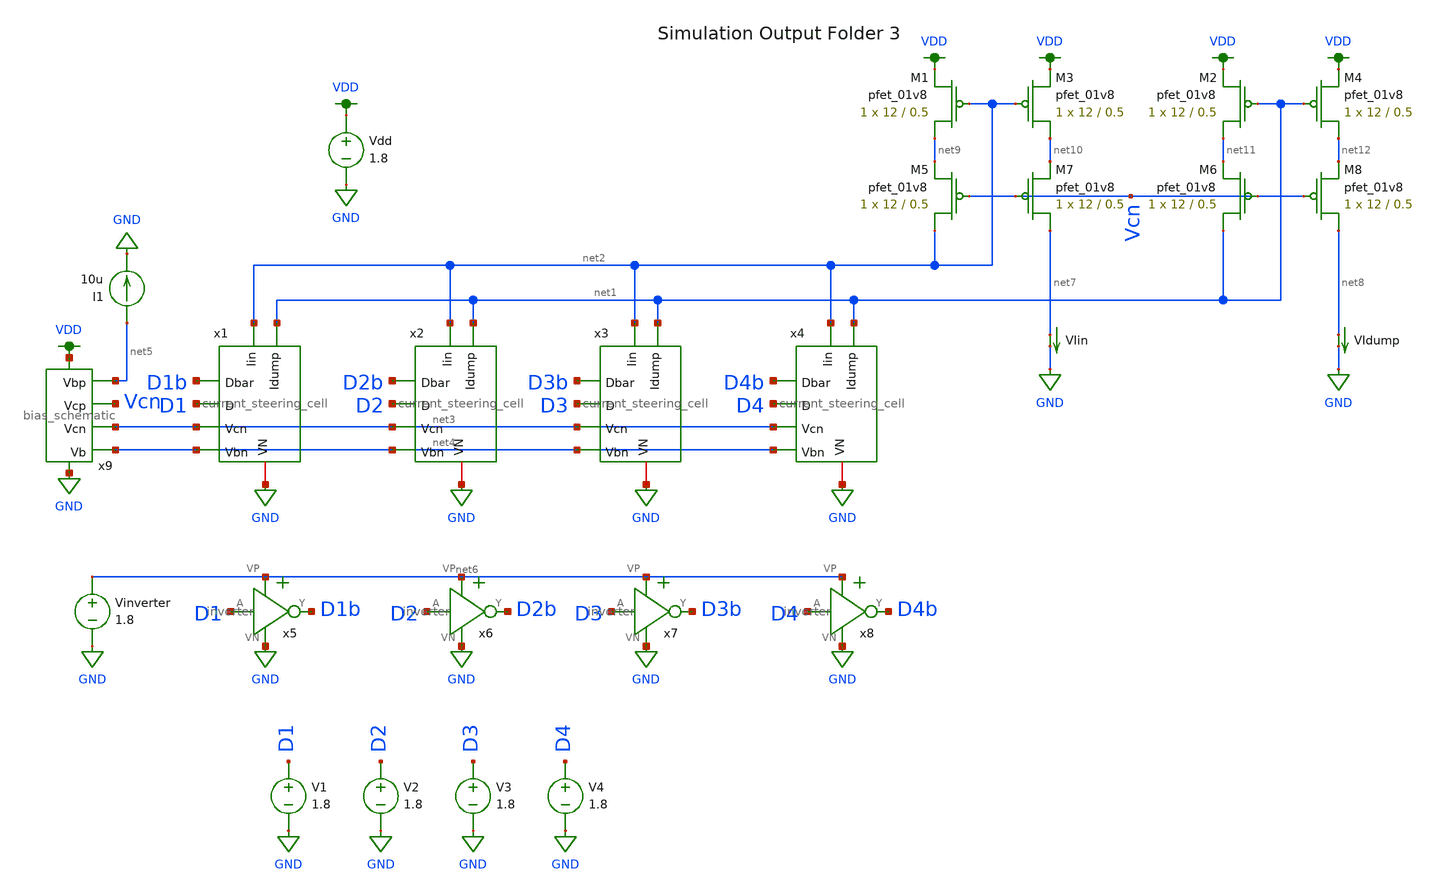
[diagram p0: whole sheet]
** sch_path: xschem/current_steering_testbenches/current_steering_testbench_pmos_cascode_mirror.sch
**.subckt current_steering_testbench_pmos_cascode_mirror
V1 D1 GND 1.8
V2 D2 GND 1.8
V3 D3 GND 1.8
V4 D4 GND 1.8
I1 net5 GND 10u
VIin net7 GND 0
.save i(viin)
VIdump net8 GND 0
.save i(vidump)
Vdd VDD GND 1.8
Vinverter net6 GND 1.8
XM1 net9 net2 VDD VDD sky130_fd_pr__pfet_01v8 L=0.5 W=12 nf=1 ad='int((nf+1)/2) * W/nf * 0.29' as='int((nf+2)/2) * W/nf * 0.29'
+ pd='2*int((nf+1)/2) * (W/nf + 0.29)' ps='2*int((nf+2)/2) * (W/nf + 0.29)' nrd='0.29 / W' nrs='0.29 / W'
+ sa=0 sb=0 sd=0 mult=1 m=1
XM2 net11 net1 VDD VDD sky130_fd_pr__pfet_01v8 L=0.5 W=12 nf=1 ad='int((nf+1)/2) * W/nf * 0.29' as='int((nf+2)/2) * W/nf * 0.29'
+ pd='2*int((nf+1)/2) * (W/nf + 0.29)' ps='2*int((nf+2)/2) * (W/nf + 0.29)' nrd='0.29 / W' nrs='0.29 / W'
+ sa=0 sb=0 sd=0 mult=1 m=1
XM3 net10 net2 VDD VDD sky130_fd_pr__pfet_01v8 L=0.5 W=12 nf=1 ad='int((nf+1)/2) * W/nf * 0.29' as='int((nf+2)/2) * W/nf * 0.29'
+ pd='2*int((nf+1)/2) * (W/nf + 0.29)' ps='2*int((nf+2)/2) * (W/nf + 0.29)' nrd='0.29 / W' nrs='0.29 / W'
+ sa=0 sb=0 sd=0 mult=1 m=1
XM4 net12 net1 VDD VDD sky130_fd_pr__pfet_01v8 L=0.5 W=12 nf=1 ad='int((nf+1)/2) * W/nf * 0.29' as='int((nf+2)/2) * W/nf * 0.29'
+ pd='2*int((nf+1)/2) * (W/nf + 0.29)' ps='2*int((nf+2)/2) * (W/nf + 0.29)' nrd='0.29 / W' nrs='0.29 / W'
+ sa=0 sb=0 sd=0 mult=1 m=1
XM5 net2 Vcn net9 VDD sky130_fd_pr__pfet_01v8 L=0.5 W=12 nf=1 ad='int((nf+1)/2) * W/nf * 0.29' as='int((nf+2)/2) * W/nf * 0.29'
+ pd='2*int((nf+1)/2) * (W/nf + 0.29)' ps='2*int((nf+2)/2) * (W/nf + 0.29)' nrd='0.29 / W' nrs='0.29 / W'
+ sa=0 sb=0 sd=0 mult=1 m=1
XM6 net1 Vcn net11 VDD sky130_fd_pr__pfet_01v8 L=0.5 W=12 nf=1 ad='int((nf+1)/2) * W/nf * 0.29' as='int((nf+2)/2) * W/nf * 0.29'
+ pd='2*int((nf+1)/2) * (W/nf + 0.29)' ps='2*int((nf+2)/2) * (W/nf + 0.29)' nrd='0.29 / W' nrs='0.29 / W'
+ sa=0 sb=0 sd=0 mult=1 m=1
XM7 net7 Vcn net10 VDD sky130_fd_pr__pfet_01v8 L=0.5 W=12 nf=1 ad='int((nf+1)/2) * W/nf * 0.29' as='int((nf+2)/2) * W/nf * 0.29'
+ pd='2*int((nf+1)/2) * (W/nf + 0.29)' ps='2*int((nf+2)/2) * (W/nf + 0.29)' nrd='0.29 / W' nrs='0.29 / W'
+ sa=0 sb=0 sd=0 mult=1 m=1
XM8 net8 Vcn net12 VDD sky130_fd_pr__pfet_01v8 L=0.5 W=12 nf=1 ad='int((nf+1)/2) * W/nf * 0.29' as='int((nf+2)/2) * W/nf * 0.29'
+ pd='2*int((nf+1)/2) * (W/nf + 0.29)' ps='2*int((nf+2)/2) * (W/nf + 0.29)' nrd='0.29 / W' nrs='0.29 / W'
+ sa=0 sb=0 sd=0 mult=1 m=1
x1 net2 net1 D1b D1 net3 net4 GND current_steering_cell
x2 net2 net1 D2b D2 net3 net4 GND current_steering_cell
x3 net2 net1 D3b D3 net3 net4 GND current_steering_cell
x4 net2 net1 D4b D4 net3 net4 GND current_steering_cell
x5 net6 D1 D1b GND inverter
x6 net6 D2 D2b GND inverter
x7 net6 D3 D3b GND inverter
x8 net6 D4 D4b GND inverter
x9 VDD net5 Vcn net3 GND net4 bias_schematic
**** begin user architecture code

.save all
.control
set wr_vecnames
set wr_singlescale

let mc_runs = 10
let run = 1
dowhile run <= mc_runs

  let code = 0
  while code <= 4
    let d1 = code >= 1
    let d2 = code >= 2
    let d3 = code >= 3
    let d4 = code >= 4

    alter V1 $&d1
    alter V2 $&d2
    alter V3 $&d3
    alter V4 $&d4
    save all
    op

    wrdata ~/dev/git/magic-dds/simulations/current_steering_dac/3/ieeeDAC_{$&run}.txt code v(D1) v(D1b)
+ i(VIin) i(VIdump)
    if code eq 0
      set appendwrite
      set wr_vecnames = FALSE
    end
    let code = code + 1
  end
  reset
  set appendwrite = FALSE
  set wr_vecnames
  let run = run + 1
end
.endc


.option wnflag=1
.param MC_SWITCH=1.0
.lib ~/skywater/skywater-pdk/libraries/sky130_fd_pr_ngspice/latest/models/sky130.lib.spice tt

**** end user architecture code
**.ends

* expanding   symbol:  /home/madvlsi/dev/git/magic-dds/xschem/current_steering_cell.sym # of pins=7
** sym_path: xschem/current_steering_cell.sym
** sch_path: xschem/current_steering_cell.sch
.subckt current_steering_cell Iin Idump Dbar D Vcn Vbn VN
*.iopin VN
*.ipin D
*.ipin Dbar
*.ipin Vcn
*.ipin Iin
*.ipin Idump
*.ipin Vbn
XM1 Iin D net1 GND sky130_fd_pr__nfet_01v8 L=0.5 W=12 nf=1 ad='int((nf+1)/2) * W/nf * 0.29' as='int((nf+2)/2) * W/nf * 0.29'
+ pd='2*int((nf+1)/2) * (W/nf + 0.29)' ps='2*int((nf+2)/2) * (W/nf + 0.29)' nrd='0.29 / W' nrs='0.29 / W'
+ sa=0 sb=0 sd=0 mult=1 m=1
XM2 Idump Dbar net1 GND sky130_fd_pr__nfet_01v8 L=0.5 W=12 nf=1 ad='int((nf+1)/2) * W/nf * 0.29' as='int((nf+2)/2) * W/nf * 0.29'
+ pd='2*int((nf+1)/2) * (W/nf + 0.29)' ps='2*int((nf+2)/2) * (W/nf + 0.29)' nrd='0.29 / W' nrs='0.29 / W'
+ sa=0 sb=0 sd=0 mult=1 m=1
XM3 net2 Vbn VN GND sky130_fd_pr__nfet_01v8 L=0.5 W=12 nf=1 ad='int((nf+1)/2) * W/nf * 0.29' as='int((nf+2)/2) * W/nf * 0.29'
+ pd='2*int((nf+1)/2) * (W/nf + 0.29)' ps='2*int((nf+2)/2) * (W/nf + 0.29)' nrd='0.29 / W' nrs='0.29 / W'
+ sa=0 sb=0 sd=0 mult=1 m=1
XM4 net1 Vcn net2 GND sky130_fd_pr__nfet_01v8 L=0.5 W=12 nf=1 ad='int((nf+1)/2) * W/nf * 0.29' as='int((nf+2)/2) * W/nf * 0.29'
+ pd='2*int((nf+1)/2) * (W/nf + 0.29)' ps='2*int((nf+2)/2) * (W/nf + 0.29)' nrd='0.29 / W' nrs='0.29 / W'
+ sa=0 sb=0 sd=0 mult=1 m=1
.ends


* expanding   symbol:  /home/madvlsi/dev/git/magic-dds/xschem/other_project_files/inverter.sym # of
*+ pins=4
** sym_path: xschem/other_project_files/inverter.sym
** sch_path: xschem/other_project_files/inverter.sch
.subckt inverter VP A Y VN
*.iopin VP
*.iopin VN
*.ipin A
*.opin Y
XM1 Y A VN VN sky130_fd_pr__nfet_01v8 L=0.15 W=1 nf=1 ad='int((nf+1)/2) * W/nf * 0.29' as='int((nf+2)/2) * W/nf * 0.29'
+ pd='2*int((nf+1)/2) * (W/nf + 0.29)' ps='2*int((nf+2)/2) * (W/nf + 0.29)' nrd='0.29 / W' nrs='0.29 / W'
+ sa=0 sb=0 sd=0 mult=1 m=1
XM2 Y A VP VP sky130_fd_pr__pfet_01v8 L=0.15 W=4 nf=1 ad='int((nf+1)/2) * W/nf * 0.29' as='int((nf+2)/2) * W/nf * 0.29'
+ pd='2*int((nf+1)/2) * (W/nf + 0.29)' ps='2*int((nf+2)/2) * (W/nf + 0.29)' nrd='0.29 / W' nrs='0.29 / W'
+ sa=0 sb=0 sd=0 mult=1 m=1
.ends


* expanding   symbol:  /home/madvlsi/dev/git/magic-dds/xschem/other_project_files/bias_schematic.sym
*+ # of pins=6
** sym_path: xschem/other_project_files/bias_schematic.sym
** sch_path: xschem/other_project_files/bias_schematic.sch
.subckt bias_schematic VP Vbp Vcp Vcn VN Vb
*.iopin VP
*.iopin VN
*.opin Vcp
*.iopin Vbp
*.opin Vcn
*.opin Vb
XM1a net2 net2 net1 GND sky130_fd_pr__nfet_01v8 L=0.5 W=3 nf=1 ad='int((nf+1)/2) * W/nf * 0.29' as='int((nf+2)/2) * W/nf * 0.29'
+ pd='2*int((nf+1)/2) * (W/nf + 0.29)' ps='2*int((nf+2)/2) * (W/nf + 0.29)' nrd='0.29 / W' nrs='0.29 / W'
+ sa=0 sb=0 sd=0 mult=1 m=1
XM1b net2 net2 net1 GND sky130_fd_pr__nfet_01v8 L=0.5 W=3 nf=1 ad='int((nf+1)/2) * W/nf * 0.29' as='int((nf+2)/2) * W/nf * 0.29'
+ pd='2*int((nf+1)/2) * (W/nf + 0.29)' ps='2*int((nf+2)/2) * (W/nf + 0.29)' nrd='0.29 / W' nrs='0.29 / W'
+ sa=0 sb=0 sd=0 mult=1 m=1
XM1c net2 net2 net1 GND sky130_fd_pr__nfet_01v8 L=0.5 W=3 nf=1 ad='int((nf+1)/2) * W/nf * 0.29' as='int((nf+2)/2) * W/nf * 0.29'
+ pd='2*int((nf+1)/2) * (W/nf + 0.29)' ps='2*int((nf+2)/2) * (W/nf + 0.29)' nrd='0.29 / W' nrs='0.29 / W'
+ sa=0 sb=0 sd=0 mult=1 m=1
XM1d net2 net2 net1 GND sky130_fd_pr__nfet_01v8 L=0.5 W=3 nf=1 ad='int((nf+1)/2) * W/nf * 0.29' as='int((nf+2)/2) * W/nf * 0.29'
+ pd='2*int((nf+1)/2) * (W/nf + 0.29)' ps='2*int((nf+2)/2) * (W/nf + 0.29)' nrd='0.29 / W' nrs='0.29 / W'
+ sa=0 sb=0 sd=0 mult=1 m=1
XM2a VN net2 net1 GND sky130_fd_pr__nfet_01v8 L=0.5 W=3 nf=1 ad='int((nf+1)/2) * W/nf * 0.29' as='int((nf+2)/2) * W/nf * 0.29'
+ pd='2*int((nf+1)/2) * (W/nf + 0.29)' ps='2*int((nf+2)/2) * (W/nf + 0.29)' nrd='0.29 / W' nrs='0.29 / W'
+ sa=0 sb=0 sd=0 mult=1 m=1
XM2b VN net2 net1 GND sky130_fd_pr__nfet_01v8 L=0.5 W=3 nf=1 ad='int((nf+1)/2) * W/nf * 0.29' as='int((nf+2)/2) * W/nf * 0.29'
+ pd='2*int((nf+1)/2) * (W/nf + 0.29)' ps='2*int((nf+2)/2) * (W/nf + 0.29)' nrd='0.29 / W' nrs='0.29 / W'
+ sa=0 sb=0 sd=0 mult=1 m=1
XM2c VN net2 net1 GND sky130_fd_pr__nfet_01v8 L=0.5 W=3 nf=1 ad='int((nf+1)/2) * W/nf * 0.29' as='int((nf+2)/2) * W/nf * 0.29'
+ pd='2*int((nf+1)/2) * (W/nf + 0.29)' ps='2*int((nf+2)/2) * (W/nf + 0.29)' nrd='0.29 / W' nrs='0.29 / W'
+ sa=0 sb=0 sd=0 mult=1 m=1
XM2d VN net2 net1 GND sky130_fd_pr__nfet_01v8 L=0.5 W=3 nf=1 ad='int((nf+1)/2) * W/nf * 0.29' as='int((nf+2)/2) * W/nf * 0.29'
+ pd='2*int((nf+1)/2) * (W/nf + 0.29)' ps='2*int((nf+2)/2) * (W/nf + 0.29)' nrd='0.29 / W' nrs='0.29 / W'
+ sa=0 sb=0 sd=0 mult=1 m=1
XM3a net2 Vbp net7 VDD sky130_fd_pr__pfet_01v8 L=0.5 W=3 nf=1 ad='int((nf+1)/2) * W/nf * 0.29' as='int((nf+2)/2) * W/nf * 0.29'
+ pd='2*int((nf+1)/2) * (W/nf + 0.29)' ps='2*int((nf+2)/2) * (W/nf + 0.29)' nrd='0.29 / W' nrs='0.29 / W'
+ sa=0 sb=0 sd=0 mult=1 m=1
XM3b net7 Vbp net6 VDD sky130_fd_pr__pfet_01v8 L=0.5 W=3 nf=1 ad='int((nf+1)/2) * W/nf * 0.29' as='int((nf+2)/2) * W/nf * 0.29'
+ pd='2*int((nf+1)/2) * (W/nf + 0.29)' ps='2*int((nf+2)/2) * (W/nf + 0.29)' nrd='0.29 / W' nrs='0.29 / W'
+ sa=0 sb=0 sd=0 mult=1 m=1
XM3c net6 Vbp net5 VDD sky130_fd_pr__pfet_01v8 L=0.5 W=3 nf=1 ad='int((nf+1)/2) * W/nf * 0.29' as='int((nf+2)/2) * W/nf * 0.29'
+ pd='2*int((nf+1)/2) * (W/nf + 0.29)' ps='2*int((nf+2)/2) * (W/nf + 0.29)' nrd='0.29 / W' nrs='0.29 / W'
+ sa=0 sb=0 sd=0 mult=1 m=1
XM3d net5 Vbp VP VDD sky130_fd_pr__pfet_01v8 L=0.5 W=3 nf=1 ad='int((nf+1)/2) * W/nf * 0.29' as='int((nf+2)/2) * W/nf * 0.29'
+ pd='2*int((nf+1)/2) * (W/nf + 0.29)' ps='2*int((nf+2)/2) * (W/nf + 0.29)' nrd='0.29 / W' nrs='0.29 / W'
+ sa=0 sb=0 sd=0 mult=1 m=1
XM4a Vcn Vbp VP VDD sky130_fd_pr__pfet_01v8 L=0.5 W=3 nf=1 ad='int((nf+1)/2) * W/nf * 0.29' as='int((nf+2)/2) * W/nf * 0.29'
+ pd='2*int((nf+1)/2) * (W/nf + 0.29)' ps='2*int((nf+2)/2) * (W/nf + 0.29)' nrd='0.29 / W' nrs='0.29 / W'
+ sa=0 sb=0 sd=0 mult=1 m=1
XM4b Vcn Vbp VP VDD sky130_fd_pr__pfet_01v8 L=0.5 W=3 nf=1 ad='int((nf+1)/2) * W/nf * 0.29' as='int((nf+2)/2) * W/nf * 0.29'
+ pd='2*int((nf+1)/2) * (W/nf + 0.29)' ps='2*int((nf+2)/2) * (W/nf + 0.29)' nrd='0.29 / W' nrs='0.29 / W'
+ sa=0 sb=0 sd=0 mult=1 m=1
XM4c Vcn Vbp VP VDD sky130_fd_pr__pfet_01v8 L=0.5 W=3 nf=1 ad='int((nf+1)/2) * W/nf * 0.29' as='int((nf+2)/2) * W/nf * 0.29'
+ pd='2*int((nf+1)/2) * (W/nf + 0.29)' ps='2*int((nf+2)/2) * (W/nf + 0.29)' nrd='0.29 / W' nrs='0.29 / W'
+ sa=0 sb=0 sd=0 mult=1 m=1
XM4d Vcn Vbp VP VDD sky130_fd_pr__pfet_01v8 L=0.5 W=3 nf=1 ad='int((nf+1)/2) * W/nf * 0.29' as='int((nf+2)/2) * W/nf * 0.29'
+ pd='2*int((nf+1)/2) * (W/nf + 0.29)' ps='2*int((nf+2)/2) * (W/nf + 0.29)' nrd='0.29 / W' nrs='0.29 / W'
+ sa=0 sb=0 sd=0 mult=1 m=1
XM11a VP Vbp Vbp VDD sky130_fd_pr__pfet_01v8 L=0.5 W=3 nf=1 ad='int((nf+1)/2) * W/nf * 0.29' as='int((nf+2)/2) * W/nf * 0.29'
+ pd='2*int((nf+1)/2) * (W/nf + 0.29)' ps='2*int((nf+2)/2) * (W/nf + 0.29)' nrd='0.29 / W' nrs='0.29 / W'
+ sa=0 sb=0 sd=0 mult=1 m=1
XM11b VP Vbp Vbp VDD sky130_fd_pr__pfet_01v8 L=0.5 W=3 nf=1 ad='int((nf+1)/2) * W/nf * 0.29' as='int((nf+2)/2) * W/nf * 0.29'
+ pd='2*int((nf+1)/2) * (W/nf + 0.29)' ps='2*int((nf+2)/2) * (W/nf + 0.29)' nrd='0.29 / W' nrs='0.29 / W'
+ sa=0 sb=0 sd=0 mult=1 m=1
XM11c VP Vbp Vbp VDD sky130_fd_pr__pfet_01v8 L=0.5 W=3 nf=1 ad='int((nf+1)/2) * W/nf * 0.29' as='int((nf+2)/2) * W/nf * 0.29'
+ pd='2*int((nf+1)/2) * (W/nf + 0.29)' ps='2*int((nf+2)/2) * (W/nf + 0.29)' nrd='0.29 / W' nrs='0.29 / W'
+ sa=0 sb=0 sd=0 mult=1 m=1
XM11d VP Vbp Vbp VDD sky130_fd_pr__pfet_01v8 L=0.5 W=3 nf=1 ad='int((nf+1)/2) * W/nf * 0.29' as='int((nf+2)/2) * W/nf * 0.29'
+ pd='2*int((nf+1)/2) * (W/nf + 0.29)' ps='2*int((nf+2)/2) * (W/nf + 0.29)' nrd='0.29 / W' nrs='0.29 / W'
+ sa=0 sb=0 sd=0 mult=1 m=1
XM5a net1 Vcn Vcn GND sky130_fd_pr__nfet_01v8 L=0.5 W=3 nf=1 ad='int((nf+1)/2) * W/nf * 0.29' as='int((nf+2)/2) * W/nf * 0.29'
+ pd='2*int((nf+1)/2) * (W/nf + 0.29)' ps='2*int((nf+2)/2) * (W/nf + 0.29)' nrd='0.29 / W' nrs='0.29 / W'
+ sa=0 sb=0 sd=0 mult=1 m=1
XM5b net1 Vcn Vcn GND sky130_fd_pr__nfet_01v8 L=0.5 W=3 nf=1 ad='int((nf+1)/2) * W/nf * 0.29' as='int((nf+2)/2) * W/nf * 0.29'
+ pd='2*int((nf+1)/2) * (W/nf + 0.29)' ps='2*int((nf+2)/2) * (W/nf + 0.29)' nrd='0.29 / W' nrs='0.29 / W'
+ sa=0 sb=0 sd=0 mult=1 m=1
XM5c net1 Vcn Vcn GND sky130_fd_pr__nfet_01v8 L=0.5 W=3 nf=1 ad='int((nf+1)/2) * W/nf * 0.29' as='int((nf+2)/2) * W/nf * 0.29'
+ pd='2*int((nf+1)/2) * (W/nf + 0.29)' ps='2*int((nf+2)/2) * (W/nf + 0.29)' nrd='0.29 / W' nrs='0.29 / W'
+ sa=0 sb=0 sd=0 mult=1 m=1
XM5d net1 Vcn Vcn GND sky130_fd_pr__nfet_01v8 L=0.5 W=3 nf=1 ad='int((nf+1)/2) * W/nf * 0.29' as='int((nf+2)/2) * W/nf * 0.29'
+ pd='2*int((nf+1)/2) * (W/nf + 0.29)' ps='2*int((nf+2)/2) * (W/nf + 0.29)' nrd='0.29 / W' nrs='0.29 / W'
+ sa=0 sb=0 sd=0 mult=1 m=1
XM8a net10 Vb net3 GND sky130_fd_pr__nfet_01v8 L=0.5 W=3 nf=1 ad='int((nf+1)/2) * W/nf * 0.29' as='int((nf+2)/2) * W/nf * 0.29'
+ pd='2*int((nf+1)/2) * (W/nf + 0.29)' ps='2*int((nf+2)/2) * (W/nf + 0.29)' nrd='0.29 / W' nrs='0.29 / W'
+ sa=0 sb=0 sd=0 mult=1 m=1
XM8b net9 Vb net10 GND sky130_fd_pr__nfet_01v8 L=0.5 W=3 nf=1 ad='int((nf+1)/2) * W/nf * 0.29' as='int((nf+2)/2) * W/nf * 0.29'
+ pd='2*int((nf+1)/2) * (W/nf + 0.29)' ps='2*int((nf+2)/2) * (W/nf + 0.29)' nrd='0.29 / W' nrs='0.29 / W'
+ sa=0 sb=0 sd=0 mult=1 m=1
XM8c net8 Vb net9 GND sky130_fd_pr__nfet_01v8 L=0.5 W=3 nf=1 ad='int((nf+1)/2) * W/nf * 0.29' as='int((nf+2)/2) * W/nf * 0.29'
+ pd='2*int((nf+1)/2) * (W/nf + 0.29)' ps='2*int((nf+2)/2) * (W/nf + 0.29)' nrd='0.29 / W' nrs='0.29 / W'
+ sa=0 sb=0 sd=0 mult=1 m=1
XM8d VN Vb net8 GND sky130_fd_pr__nfet_01v8 L=0.5 W=3 nf=1 ad='int((nf+1)/2) * W/nf * 0.29' as='int((nf+2)/2) * W/nf * 0.29'
+ pd='2*int((nf+1)/2) * (W/nf + 0.29)' ps='2*int((nf+2)/2) * (W/nf + 0.29)' nrd='0.29 / W' nrs='0.29 / W'
+ sa=0 sb=0 sd=0 mult=1 m=1
XM6a net3 net3 net4 VDD sky130_fd_pr__pfet_01v8 L=0.5 W=3 nf=1 ad='int((nf+1)/2) * W/nf * 0.29' as='int((nf+2)/2) * W/nf * 0.29'
+ pd='2*int((nf+1)/2) * (W/nf + 0.29)' ps='2*int((nf+2)/2) * (W/nf + 0.29)' nrd='0.29 / W' nrs='0.29 / W'
+ sa=0 sb=0 sd=0 mult=1 m=1
XM6b net3 net3 net4 VDD sky130_fd_pr__pfet_01v8 L=0.5 W=3 nf=1 ad='int((nf+1)/2) * W/nf * 0.29' as='int((nf+2)/2) * W/nf * 0.29'
+ pd='2*int((nf+1)/2) * (W/nf + 0.29)' ps='2*int((nf+2)/2) * (W/nf + 0.29)' nrd='0.29 / W' nrs='0.29 / W'
+ sa=0 sb=0 sd=0 mult=1 m=1
XM6c net3 net3 net4 VDD sky130_fd_pr__pfet_01v8 L=0.5 W=3 nf=1 ad='int((nf+1)/2) * W/nf * 0.29' as='int((nf+2)/2) * W/nf * 0.29'
+ pd='2*int((nf+1)/2) * (W/nf + 0.29)' ps='2*int((nf+2)/2) * (W/nf + 0.29)' nrd='0.29 / W' nrs='0.29 / W'
+ sa=0 sb=0 sd=0 mult=1 m=1
XM6d net3 net3 net4 VDD sky130_fd_pr__pfet_01v8 L=0.5 W=3 nf=1 ad='int((nf+1)/2) * W/nf * 0.29' as='int((nf+2)/2) * W/nf * 0.29'
+ pd='2*int((nf+1)/2) * (W/nf + 0.29)' ps='2*int((nf+2)/2) * (W/nf + 0.29)' nrd='0.29 / W' nrs='0.29 / W'
+ sa=0 sb=0 sd=0 mult=1 m=1
XM7a net4 net3 VP VDD sky130_fd_pr__pfet_01v8 L=0.5 W=3 nf=1 ad='int((nf+1)/2) * W/nf * 0.29' as='int((nf+2)/2) * W/nf * 0.29'
+ pd='2*int((nf+1)/2) * (W/nf + 0.29)' ps='2*int((nf+2)/2) * (W/nf + 0.29)' nrd='0.29 / W' nrs='0.29 / W'
+ sa=0 sb=0 sd=0 mult=1 m=1
XM7b net4 net3 VP VDD sky130_fd_pr__pfet_01v8 L=0.5 W=3 nf=1 ad='int((nf+1)/2) * W/nf * 0.29' as='int((nf+2)/2) * W/nf * 0.29'
+ pd='2*int((nf+1)/2) * (W/nf + 0.29)' ps='2*int((nf+2)/2) * (W/nf + 0.29)' nrd='0.29 / W' nrs='0.29 / W'
+ sa=0 sb=0 sd=0 mult=1 m=1
XM7c net4 net3 VP VDD sky130_fd_pr__pfet_01v8 L=0.5 W=3 nf=1 ad='int((nf+1)/2) * W/nf * 0.29' as='int((nf+2)/2) * W/nf * 0.29'
+ pd='2*int((nf+1)/2) * (W/nf + 0.29)' ps='2*int((nf+2)/2) * (W/nf + 0.29)' nrd='0.29 / W' nrs='0.29 / W'
+ sa=0 sb=0 sd=0 mult=1 m=1
XM7d net4 net3 VP VDD sky130_fd_pr__pfet_01v8 L=0.5 W=3 nf=1 ad='int((nf+1)/2) * W/nf * 0.29' as='int((nf+2)/2) * W/nf * 0.29'
+ pd='2*int((nf+1)/2) * (W/nf + 0.29)' ps='2*int((nf+2)/2) * (W/nf + 0.29)' nrd='0.29 / W' nrs='0.29 / W'
+ sa=0 sb=0 sd=0 mult=1 m=1
XM10d net4 Vcp Vcp VDD sky130_fd_pr__pfet_01v8 L=0.5 W=3 nf=1 ad='int((nf+1)/2) * W/nf * 0.29' as='int((nf+2)/2) * W/nf * 0.29'
+ pd='2*int((nf+1)/2) * (W/nf + 0.29)' ps='2*int((nf+2)/2) * (W/nf + 0.29)' nrd='0.29 / W' nrs='0.29 / W'
+ sa=0 sb=0 sd=0 mult=1 m=1
XM10c net4 Vcp Vcp VDD sky130_fd_pr__pfet_01v8 L=0.5 W=3 nf=1 ad='int((nf+1)/2) * W/nf * 0.29' as='int((nf+2)/2) * W/nf * 0.29'
+ pd='2*int((nf+1)/2) * (W/nf + 0.29)' ps='2*int((nf+2)/2) * (W/nf + 0.29)' nrd='0.29 / W' nrs='0.29 / W'
+ sa=0 sb=0 sd=0 mult=1 m=1
XM10b net4 Vcp Vcp VDD sky130_fd_pr__pfet_01v8 L=0.5 W=3 nf=1 ad='int((nf+1)/2) * W/nf * 0.29' as='int((nf+2)/2) * W/nf * 0.29'
+ pd='2*int((nf+1)/2) * (W/nf + 0.29)' ps='2*int((nf+2)/2) * (W/nf + 0.29)' nrd='0.29 / W' nrs='0.29 / W'
+ sa=0 sb=0 sd=0 mult=1 m=1
XM10a net4 Vcp Vcp VDD sky130_fd_pr__pfet_01v8 L=0.5 W=3 nf=1 ad='int((nf+1)/2) * W/nf * 0.29' as='int((nf+2)/2) * W/nf * 0.29'
+ pd='2*int((nf+1)/2) * (W/nf + 0.29)' ps='2*int((nf+2)/2) * (W/nf + 0.29)' nrd='0.29 / W' nrs='0.29 / W'
+ sa=0 sb=0 sd=0 mult=1 m=1
XM9a VN Vb Vcp GND sky130_fd_pr__nfet_01v8 L=0.5 W=3 nf=1 ad='int((nf+1)/2) * W/nf * 0.29' as='int((nf+2)/2) * W/nf * 0.29'
+ pd='2*int((nf+1)/2) * (W/nf + 0.29)' ps='2*int((nf+2)/2) * (W/nf + 0.29)' nrd='0.29 / W' nrs='0.29 / W'
+ sa=0 sb=0 sd=0 mult=1 m=1
XM9b VN Vb Vcp GND sky130_fd_pr__nfet_01v8 L=0.5 W=3 nf=1 ad='int((nf+1)/2) * W/nf * 0.29' as='int((nf+2)/2) * W/nf * 0.29'
+ pd='2*int((nf+1)/2) * (W/nf + 0.29)' ps='2*int((nf+2)/2) * (W/nf + 0.29)' nrd='0.29 / W' nrs='0.29 / W'
+ sa=0 sb=0 sd=0 mult=1 m=1
XM9c VN Vb Vcp GND sky130_fd_pr__nfet_01v8 L=0.5 W=3 nf=1 ad='int((nf+1)/2) * W/nf * 0.29' as='int((nf+2)/2) * W/nf * 0.29'
+ pd='2*int((nf+1)/2) * (W/nf + 0.29)' ps='2*int((nf+2)/2) * (W/nf + 0.29)' nrd='0.29 / W' nrs='0.29 / W'
+ sa=0 sb=0 sd=0 mult=1 m=1
XM9d VN Vb Vcp GND sky130_fd_pr__nfet_01v8 L=0.5 W=3 nf=1 ad='int((nf+1)/2) * W/nf * 0.29' as='int((nf+2)/2) * W/nf * 0.29'
+ pd='2*int((nf+1)/2) * (W/nf + 0.29)' ps='2*int((nf+2)/2) * (W/nf + 0.29)' nrd='0.29 / W' nrs='0.29 / W'
+ sa=0 sb=0 sd=0 mult=1 m=1
XM12a VN Vb Vb GND sky130_fd_pr__nfet_01v8 L=0.5 W=3 nf=1 ad='int((nf+1)/2) * W/nf * 0.29' as='int((nf+2)/2) * W/nf * 0.29'
+ pd='2*int((nf+1)/2) * (W/nf + 0.29)' ps='2*int((nf+2)/2) * (W/nf + 0.29)' nrd='0.29 / W' nrs='0.29 / W'
+ sa=0 sb=0 sd=0 mult=1 m=1
XM12b VN Vb Vb GND sky130_fd_pr__nfet_01v8 L=0.5 W=3 nf=1 ad='int((nf+1)/2) * W/nf * 0.29' as='int((nf+2)/2) * W/nf * 0.29'
+ pd='2*int((nf+1)/2) * (W/nf + 0.29)' ps='2*int((nf+2)/2) * (W/nf + 0.29)' nrd='0.29 / W' nrs='0.29 / W'
+ sa=0 sb=0 sd=0 mult=1 m=1
XM12c VN Vb Vb GND sky130_fd_pr__nfet_01v8 L=0.5 W=3 nf=1 ad='int((nf+1)/2) * W/nf * 0.29' as='int((nf+2)/2) * W/nf * 0.29'
+ pd='2*int((nf+1)/2) * (W/nf + 0.29)' ps='2*int((nf+2)/2) * (W/nf + 0.29)' nrd='0.29 / W' nrs='0.29 / W'
+ sa=0 sb=0 sd=0 mult=1 m=1
XM12d VN Vb Vb GND sky130_fd_pr__nfet_01v8 L=0.5 W=3 nf=1 ad='int((nf+1)/2) * W/nf * 0.29' as='int((nf+2)/2) * W/nf * 0.29'
+ pd='2*int((nf+1)/2) * (W/nf + 0.29)' ps='2*int((nf+2)/2) * (W/nf + 0.29)' nrd='0.29 / W' nrs='0.29 / W'
+ sa=0 sb=0 sd=0 mult=1 m=1
XM1 Vb Vbp VP VDD sky130_fd_pr__pfet_01v8 L=0.5 W=3 nf=1 ad='int((nf+1)/2) * W/nf * 0.29' as='int((nf+2)/2) * W/nf * 0.29'
+ pd='2*int((nf+1)/2) * (W/nf + 0.29)' ps='2*int((nf+2)/2) * (W/nf + 0.29)' nrd='0.29 / W' nrs='0.29 / W'
+ sa=0 sb=0 sd=0 mult=1 m=1
XM2 Vb Vbp VP VDD sky130_fd_pr__pfet_01v8 L=0.5 W=3 nf=1 ad='int((nf+1)/2) * W/nf * 0.29' as='int((nf+2)/2) * W/nf * 0.29'
+ pd='2*int((nf+1)/2) * (W/nf + 0.29)' ps='2*int((nf+2)/2) * (W/nf + 0.29)' nrd='0.29 / W' nrs='0.29 / W'
+ sa=0 sb=0 sd=0 mult=1 m=1
XM3 Vb Vbp VP VDD sky130_fd_pr__pfet_01v8 L=0.5 W=3 nf=1 ad='int((nf+1)/2) * W/nf * 0.29' as='int((nf+2)/2) * W/nf * 0.29'
+ pd='2*int((nf+1)/2) * (W/nf + 0.29)' ps='2*int((nf+2)/2) * (W/nf + 0.29)' nrd='0.29 / W' nrs='0.29 / W'
+ sa=0 sb=0 sd=0 mult=1 m=1
XM4 Vb Vbp VP VDD sky130_fd_pr__pfet_01v8 L=0.5 W=3 nf=1 ad='int((nf+1)/2) * W/nf * 0.29' as='int((nf+2)/2) * W/nf * 0.29'
+ pd='2*int((nf+1)/2) * (W/nf + 0.29)' ps='2*int((nf+2)/2) * (W/nf + 0.29)' nrd='0.29 / W' nrs='0.29 / W'
+ sa=0 sb=0 sd=0 mult=1 m=1
XM1e net2 net2 net1 GND sky130_fd_pr__nfet_01v8 L=0.5 W=3 nf=1 ad='int((nf+1)/2) * W/nf * 0.29' as='int((nf+2)/2) * W/nf * 0.29'
+ pd='2*int((nf+1)/2) * (W/nf + 0.29)' ps='2*int((nf+2)/2) * (W/nf + 0.29)' nrd='0.29 / W' nrs='0.29 / W'
+ sa=0 sb=0 sd=0 mult=1 m=1
XM1f net2 net2 net1 GND sky130_fd_pr__nfet_01v8 L=0.5 W=3 nf=1 ad='int((nf+1)/2) * W/nf * 0.29' as='int((nf+2)/2) * W/nf * 0.29'
+ pd='2*int((nf+1)/2) * (W/nf + 0.29)' ps='2*int((nf+2)/2) * (W/nf + 0.29)' nrd='0.29 / W' nrs='0.29 / W'
+ sa=0 sb=0 sd=0 mult=1 m=1
XM1g net2 net2 net1 GND sky130_fd_pr__nfet_01v8 L=0.5 W=3 nf=1 ad='int((nf+1)/2) * W/nf * 0.29' as='int((nf+2)/2) * W/nf * 0.29'
+ pd='2*int((nf+1)/2) * (W/nf + 0.29)' ps='2*int((nf+2)/2) * (W/nf + 0.29)' nrd='0.29 / W' nrs='0.29 / W'
+ sa=0 sb=0 sd=0 mult=1 m=1
XM1h net2 net2 net1 GND sky130_fd_pr__nfet_01v8 L=0.5 W=3 nf=1 ad='int((nf+1)/2) * W/nf * 0.29' as='int((nf+2)/2) * W/nf * 0.29'
+ pd='2*int((nf+1)/2) * (W/nf + 0.29)' ps='2*int((nf+2)/2) * (W/nf + 0.29)' nrd='0.29 / W' nrs='0.29 / W'
+ sa=0 sb=0 sd=0 mult=1 m=1
XM6e net3 net3 net4 VDD sky130_fd_pr__pfet_01v8 L=0.5 W=3 nf=1 ad='int((nf+1)/2) * W/nf * 0.29' as='int((nf+2)/2) * W/nf * 0.29'
+ pd='2*int((nf+1)/2) * (W/nf + 0.29)' ps='2*int((nf+2)/2) * (W/nf + 0.29)' nrd='0.29 / W' nrs='0.29 / W'
+ sa=0 sb=0 sd=0 mult=1 m=1
XM6f net3 net3 net4 VDD sky130_fd_pr__pfet_01v8 L=0.5 W=3 nf=1 ad='int((nf+1)/2) * W/nf * 0.29' as='int((nf+2)/2) * W/nf * 0.29'
+ pd='2*int((nf+1)/2) * (W/nf + 0.29)' ps='2*int((nf+2)/2) * (W/nf + 0.29)' nrd='0.29 / W' nrs='0.29 / W'
+ sa=0 sb=0 sd=0 mult=1 m=1
XM6g net3 net3 net4 VDD sky130_fd_pr__pfet_01v8 L=0.5 W=3 nf=1 ad='int((nf+1)/2) * W/nf * 0.29' as='int((nf+2)/2) * W/nf * 0.29'
+ pd='2*int((nf+1)/2) * (W/nf + 0.29)' ps='2*int((nf+2)/2) * (W/nf + 0.29)' nrd='0.29 / W' nrs='0.29 / W'
+ sa=0 sb=0 sd=0 mult=1 m=1
XM6h net3 net3 net4 VDD sky130_fd_pr__pfet_01v8 L=0.5 W=3 nf=1 ad='int((nf+1)/2) * W/nf * 0.29' as='int((nf+2)/2) * W/nf * 0.29'
+ pd='2*int((nf+1)/2) * (W/nf + 0.29)' ps='2*int((nf+2)/2) * (W/nf + 0.29)' nrd='0.29 / W' nrs='0.29 / W'
+ sa=0 sb=0 sd=0 mult=1 m=1
XM1i net2 net2 net1 GND sky130_fd_pr__nfet_01v8 L=0.5 W=3 nf=1 ad='int((nf+1)/2) * W/nf * 0.29' as='int((nf+2)/2) * W/nf * 0.29'
+ pd='2*int((nf+1)/2) * (W/nf + 0.29)' ps='2*int((nf+2)/2) * (W/nf + 0.29)' nrd='0.29 / W' nrs='0.29 / W'
+ sa=0 sb=0 sd=0 mult=1 m=1
XM1j net2 net2 net1 GND sky130_fd_pr__nfet_01v8 L=0.5 W=3 nf=1 ad='int((nf+1)/2) * W/nf * 0.29' as='int((nf+2)/2) * W/nf * 0.29'
+ pd='2*int((nf+1)/2) * (W/nf + 0.29)' ps='2*int((nf+2)/2) * (W/nf + 0.29)' nrd='0.29 / W' nrs='0.29 / W'
+ sa=0 sb=0 sd=0 mult=1 m=1
XM1k net2 net2 net1 GND sky130_fd_pr__nfet_01v8 L=0.5 W=3 nf=1 ad='int((nf+1)/2) * W/nf * 0.29' as='int((nf+2)/2) * W/nf * 0.29'
+ pd='2*int((nf+1)/2) * (W/nf + 0.29)' ps='2*int((nf+2)/2) * (W/nf + 0.29)' nrd='0.29 / W' nrs='0.29 / W'
+ sa=0 sb=0 sd=0 mult=1 m=1
XM1l net2 net2 net1 GND sky130_fd_pr__nfet_01v8 L=0.5 W=3 nf=1 ad='int((nf+1)/2) * W/nf * 0.29' as='int((nf+2)/2) * W/nf * 0.29'
+ pd='2*int((nf+1)/2) * (W/nf + 0.29)' ps='2*int((nf+2)/2) * (W/nf + 0.29)' nrd='0.29 / W' nrs='0.29 / W'
+ sa=0 sb=0 sd=0 mult=1 m=1
XM6i net3 net3 net4 VDD sky130_fd_pr__pfet_01v8 L=0.5 W=3 nf=1 ad='int((nf+1)/2) * W/nf * 0.29' as='int((nf+2)/2) * W/nf * 0.29'
+ pd='2*int((nf+1)/2) * (W/nf + 0.29)' ps='2*int((nf+2)/2) * (W/nf + 0.29)' nrd='0.29 / W' nrs='0.29 / W'
+ sa=0 sb=0 sd=0 mult=1 m=1
XM6j net3 net3 net4 VDD sky130_fd_pr__pfet_01v8 L=0.5 W=3 nf=1 ad='int((nf+1)/2) * W/nf * 0.29' as='int((nf+2)/2) * W/nf * 0.29'
+ pd='2*int((nf+1)/2) * (W/nf + 0.29)' ps='2*int((nf+2)/2) * (W/nf + 0.29)' nrd='0.29 / W' nrs='0.29 / W'
+ sa=0 sb=0 sd=0 mult=1 m=1
XM6k net3 net3 net4 VDD sky130_fd_pr__pfet_01v8 L=0.5 W=3 nf=1 ad='int((nf+1)/2) * W/nf * 0.29' as='int((nf+2)/2) * W/nf * 0.29'
+ pd='2*int((nf+1)/2) * (W/nf + 0.29)' ps='2*int((nf+2)/2) * (W/nf + 0.29)' nrd='0.29 / W' nrs='0.29 / W'
+ sa=0 sb=0 sd=0 mult=1 m=1
XM6l net3 net3 net4 VDD sky130_fd_pr__pfet_01v8 L=0.5 W=3 nf=1 ad='int((nf+1)/2) * W/nf * 0.29' as='int((nf+2)/2) * W/nf * 0.29'
+ pd='2*int((nf+1)/2) * (W/nf + 0.29)' ps='2*int((nf+2)/2) * (W/nf + 0.29)' nrd='0.29 / W' nrs='0.29 / W'
+ sa=0 sb=0 sd=0 mult=1 m=1
.ends

.GLOBAL GND
.GLOBAL VDD
.end
